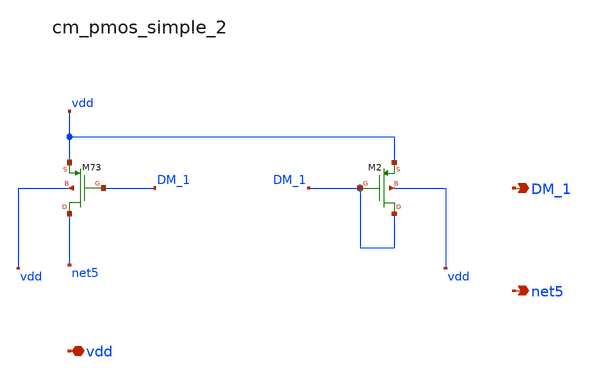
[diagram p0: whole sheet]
** sch_path: analog-db/raw/amp_017_tan_clia/hier/blocks/cm_pmos_simple_2.sch
**.subckt cm_pmos_simple_2 vdd DM_1 net5
*.iopin vdd
*.opin DM_1
*.opin net5
XM2 DM_1 DM_1 vdd vdd sg13_lv_pmos w=x_dut_xm2_w l=x_dut_xm2_l ng=1 m=x_dut_xm2_m
XM73 net5 DM_1 vdd vdd sg13_lv_pmos w=x_dut_xm73_w l=x_dut_xm73_l ng=1 m=x_dut_xm73_m
**.ends
.end
